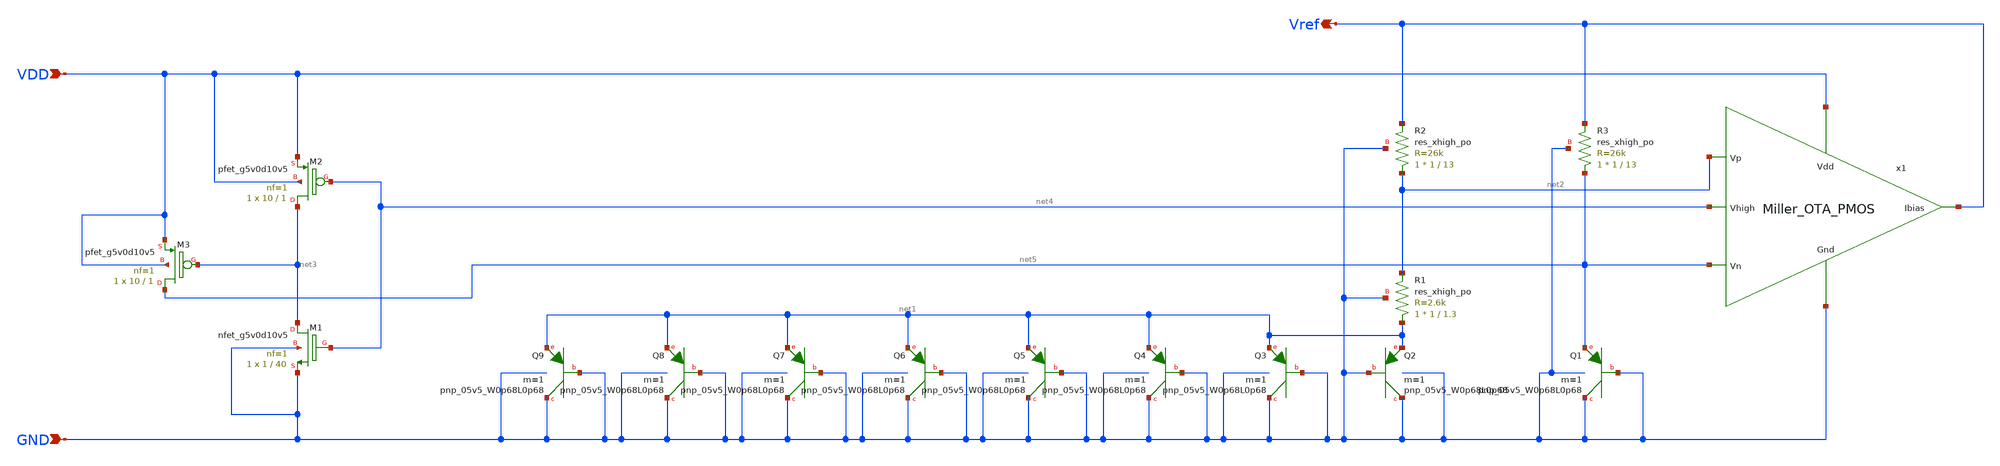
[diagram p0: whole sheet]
** sch_path: Bandgap/Schematics/BGR1.8v/Bandgap1.8v.sch
**.subckt Bandgap1.8v VDD GND Vref
*.ipin VDD
*.ipin GND
*.opin Vref
XQ1 GND GND net5 sky130_fd_pr__pnp_05v5_W0p68L0p68 m=1
XQ2 GND GND net1 sky130_fd_pr__pnp_05v5_W0p68L0p68 m=1
XQ3 GND GND net1 sky130_fd_pr__pnp_05v5_W0p68L0p68 m=1
XQ4 GND GND net1 sky130_fd_pr__pnp_05v5_W0p68L0p68 m=1
XQ5 GND GND net1 sky130_fd_pr__pnp_05v5_W0p68L0p68 m=1
XQ6 GND GND net1 sky130_fd_pr__pnp_05v5_W0p68L0p68 m=1
XQ7 GND GND net1 sky130_fd_pr__pnp_05v5_W0p68L0p68 m=1
XQ8 GND GND net1 sky130_fd_pr__pnp_05v5_W0p68L0p68 m=1
XQ9 GND GND net1 sky130_fd_pr__pnp_05v5_W0p68L0p68 m=1
XM2 net3 net4 VDD VDD sky130_fd_pr__pfet_g5v0d10v5 L=1 W=10 nf=1 ad='int((nf+1)/2) * W/nf * 0.29' as='int((nf+2)/2) * W/nf * 0.29'
+ pd='2*int((nf+1)/2) * (W/nf + 0.29)' ps='2*int((nf+2)/2) * (W/nf + 0.29)' nrd='0.29 / W' nrs='0.29 / W'
+ sa=0 sb=0 sd=0 mult=1 m=1
XM3 net5 net3 VDD VDD sky130_fd_pr__pfet_g5v0d10v5 L=1 W=10 nf=1 ad='int((nf+1)/2) * W/nf * 0.29' as='int((nf+2)/2) * W/nf * 0.29'
+ pd='2*int((nf+1)/2) * (W/nf + 0.29)' ps='2*int((nf+2)/2) * (W/nf + 0.29)' nrd='0.29 / W' nrs='0.29 / W'
+ sa=0 sb=0 sd=0 mult=1 m=1
XM1 net3 net4 GND GND sky130_fd_pr__nfet_g5v0d10v5 L=40 W=1 nf=1 ad='int((nf+1)/2) * W/nf * 0.29' as='int((nf+2)/2) * W/nf * 0.29'
+ pd='2*int((nf+1)/2) * (W/nf + 0.29)' ps='2*int((nf+2)/2) * (W/nf + 0.29)' nrd='0.29 / W' nrs='0.29 / W'
+ sa=0 sb=0 sd=0 mult=1 m=1
XR1 net1 net2 GND sky130_fd_pr__res_xhigh_po W=1 L=1.3 mult=1 m=1
XR2 net2 Vref GND sky130_fd_pr__res_xhigh_po W=1 L=13 mult=1 m=1
XR3 net5 Vref GND sky130_fd_pr__res_xhigh_po W=1 L=13 mult=1 m=1
x1 VDD net2 net5 Vref net4 GND Miller_OTA_PMOS
**.ends

* expanding   symbol:  /home/eslam/Analog_Design/Bandgap/Schematics/BGR1.8v/Miller_OTA_PMOS.sym # of
*+ pins=6
** sym_path: OTA/Schematic/Miller_OTA_PMOS.sym
** sch_path: OTA/Schematic/Miller_OTA_PMOS.sch
.subckt Miller_OTA_PMOS Vdd Vp Vn Ibias Vhigh Gnd
*.ipin Vp
*.ipin Vn
*.opin Ibias
*.ipin Vdd
*.ipin Gnd
*.ipin Vhigh
XM6 Ibias Vhigh Vdd Vdd sky130_fd_pr__pfet_g5v0d10v5 L=1 W=10 nf=1 ad='int((nf+1)/2) * W/nf * 0.29' as='int((nf+2)/2) * W/nf * 0.29'
+ pd='2*int((nf+1)/2) * (W/nf + 0.29)' ps='2*int((nf+2)/2) * (W/nf + 0.29)' nrd='0.29 / W' nrs='0.29 / W'
+ sa=0 sb=0 sd=0 mult=1 m=1
XM5 net3 Vhigh Vdd Vdd sky130_fd_pr__pfet_g5v0d10v5 L=1 W=10 nf=1 ad='int((nf+1)/2) * W/nf * 0.29' as='int((nf+2)/2) * W/nf * 0.29'
+ pd='2*int((nf+1)/2) * (W/nf + 0.29)' ps='2*int((nf+2)/2) * (W/nf + 0.29)' nrd='0.29 / W' nrs='0.29 / W'
+ sa=0 sb=0 sd=0 mult=1 m=1
XM7 Vhigh Vhigh Vdd Vdd sky130_fd_pr__pfet_g5v0d10v5 L=1 W=54 nf=1 ad='int((nf+1)/2) * W/nf * 0.29' as='int((nf+2)/2) * W/nf * 0.29'
+ pd='2*int((nf+1)/2) * (W/nf + 0.29)' ps='2*int((nf+2)/2) * (W/nf + 0.29)' nrd='0.29 / W' nrs='0.29 / W'
+ sa=0 sb=0 sd=0 mult=1 m=1
XC1 net1 Vhigh sky130_fd_pr__cap_mim_m3_2 W=1 L=1 MF=1 m=1
XM1 net2 Vn net3 Vdd sky130_fd_pr__pfet_g5v0d10v5 L=1 W=30 nf=1 ad='int((nf+1)/2) * W/nf * 0.29' as='int((nf+2)/2) * W/nf * 0.29'
+ pd='2*int((nf+1)/2) * (W/nf + 0.29)' ps='2*int((nf+2)/2) * (W/nf + 0.29)' nrd='0.29 / W' nrs='0.29 / W'
+ sa=0 sb=0 sd=0 mult=1 m=1
XM2 net1 Vp net3 Vdd sky130_fd_pr__pfet_g5v0d10v5 L=1 W=30 nf=1 ad='int((nf+1)/2) * W/nf * 0.29' as='int((nf+2)/2) * W/nf * 0.29'
+ pd='2*int((nf+1)/2) * (W/nf + 0.29)' ps='2*int((nf+2)/2) * (W/nf + 0.29)' nrd='0.29 / W' nrs='0.29 / W'
+ sa=0 sb=0 sd=0 mult=1 m=1
XM8 Vhigh net1 Gnd Gnd sky130_fd_pr__nfet_g5v0d10v5 L=0.5 W=75 nf=1 ad='int((nf+1)/2) * W/nf * 0.29'
+ as='int((nf+2)/2) * W/nf * 0.29' pd='2*int((nf+1)/2) * (W/nf + 0.29)' ps='2*int((nf+2)/2) * (W/nf + 0.29)'
+ nrd='0.29 / W' nrs='0.29 / W' sa=0 sb=0 sd=0 mult=1 m=1
XM4 net1 net2 Gnd Gnd sky130_fd_pr__nfet_g5v0d10v5 L=0.5 W=7.4 nf=1 ad='int((nf+1)/2) * W/nf * 0.29'
+ as='int((nf+2)/2) * W/nf * 0.29' pd='2*int((nf+1)/2) * (W/nf + 0.29)' ps='2*int((nf+2)/2) * (W/nf + 0.29)'
+ nrd='0.29 / W' nrs='0.29 / W' sa=0 sb=0 sd=0 mult=1 m=1
XM3 net2 net2 Gnd Gnd sky130_fd_pr__nfet_g5v0d10v5 L=0.5 W=7.4 nf=1 ad='int((nf+1)/2) * W/nf * 0.29'
+ as='int((nf+2)/2) * W/nf * 0.29' pd='2*int((nf+1)/2) * (W/nf + 0.29)' ps='2*int((nf+2)/2) * (W/nf + 0.29)'
+ nrd='0.29 / W' nrs='0.29 / W' sa=0 sb=0 sd=0 mult=1 m=1
.ends

.end
